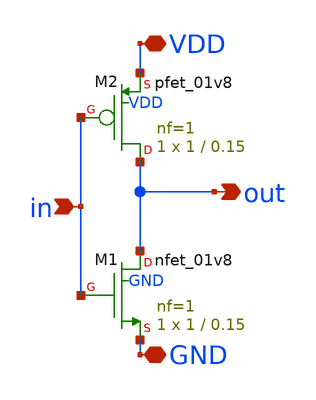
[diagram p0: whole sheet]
** sch_path: inverter.sch
**.subckt inverter out in VDD GND
*.opin out
*.ipin in
*.iopin VDD
*.iopin GND
XM1 out in GND GND sky130_fd_pr__nfet_01v8 L=0.15 W=1 nf=1 ad='int((nf+1)/2) * W/nf * 0.29' as='int((nf+2)/2) * W/nf * 0.29'
+ pd='2*int((nf+1)/2) * (W/nf + 0.29)' ps='2*int((nf+2)/2) * (W/nf + 0.29)' nrd='0.29 / W' nrs='0.29 / W'
+ sa=0 sb=0 sd=0 mult=1 m=1
XM2 out in VDD VDD sky130_fd_pr__pfet_01v8 L=0.15 W=1 nf=1 ad='int((nf+1)/2) * W/nf * 0.29' as='int((nf+2)/2) * W/nf * 0.29'
+ pd='2*int((nf+1)/2) * (W/nf + 0.29)' ps='2*int((nf+2)/2) * (W/nf + 0.29)' nrd='0.29 / W' nrs='0.29 / W'
+ sa=0 sb=0 sd=0 mult=1 m=1
**.ends
.end
